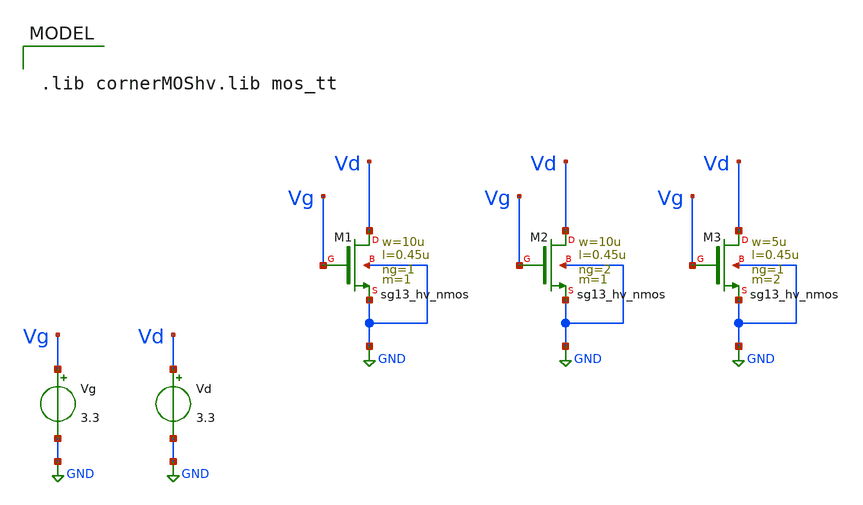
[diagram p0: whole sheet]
** sch_path: xschem/CMOS_Char/Vgs_test.sch
**.subckt Vgs_test
XM1 Vd Vg GND GND sg13_hv_nmos w=10u l=0.45u ng=1 m=1 mm_ok=1
Vg Vg GND 3.3
Vd Vd GND 3.3
XM2 Vd Vg GND GND sg13_hv_nmos w=10u l=0.45u ng=2 m=1 mm_ok=1
XM3 Vd Vg GND GND sg13_hv_nmos w=5u l=0.45u ng=1 m=2 mm_ok=1
**** begin user architecture code



.control

*** ALMACENAR DATOS Y CORRER SIMULACION

save all  @n.xm1.nsg13_hv_nmos[vgs]  @n.xm1.nsg13_hv_nmos[ids]  @n.xm2.nsg13_hv_nmos[vgs]
+  @n.xm2.nsg13_hv_nmos[ids]  @n.xm3.nsg13_hv_nmos[vgs]  @n.xm3.nsg13_hv_nmos[ids]

dc Vg 0 3.3 0.01

*** GUARDAR DATOS COMO VARIABLES Y GRAFICAR

let vgs1 = @n.xm1.nsg13_hv_nmos[vgs]
let ids1 = @n.xm1.nsg13_hv_nmos[ids]

let vgs2 = @n.xm2.nsg13_hv_nmos[vgs]
let ids2 = @n.xm2.nsg13_hv_nmos[ids]

let vgs3 = @n.xm3.nsg13_hv_nmos[vgs]
let ids3 = @n.xm3.nsg13_hv_nmos[ids]

plot ids1 vs vgs1
plot ids2 vs vgs2
plot ids3 vs vgs3

print ids1[330]
print ids2[330]
print ids3[330]
.endc



.lib cornerMOShv.lib mos_tt

**** end user architecture code
**.ends
.GLOBAL GND
.end
